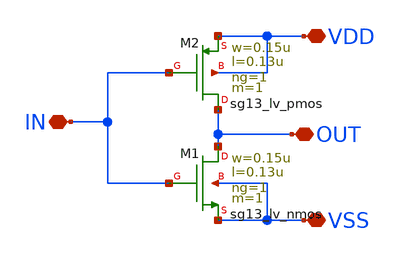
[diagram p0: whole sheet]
** sch_path: blocks/inverter/inverter.sch
**.subckt inverter VDD VSS OUT IN
*.iopin VDD
*.iopin VSS
*.iopin OUT
*.iopin IN
XM1 OUT IN VSS VSS sg13_lv_nmos w=0.15u l=0.13u ng=1 m=1 mm_ok=1
XM2 OUT IN VDD VDD sg13_lv_pmos w=0.15u l=0.13u ng=1 m=1 mm_ok=1
**.ends
.end
